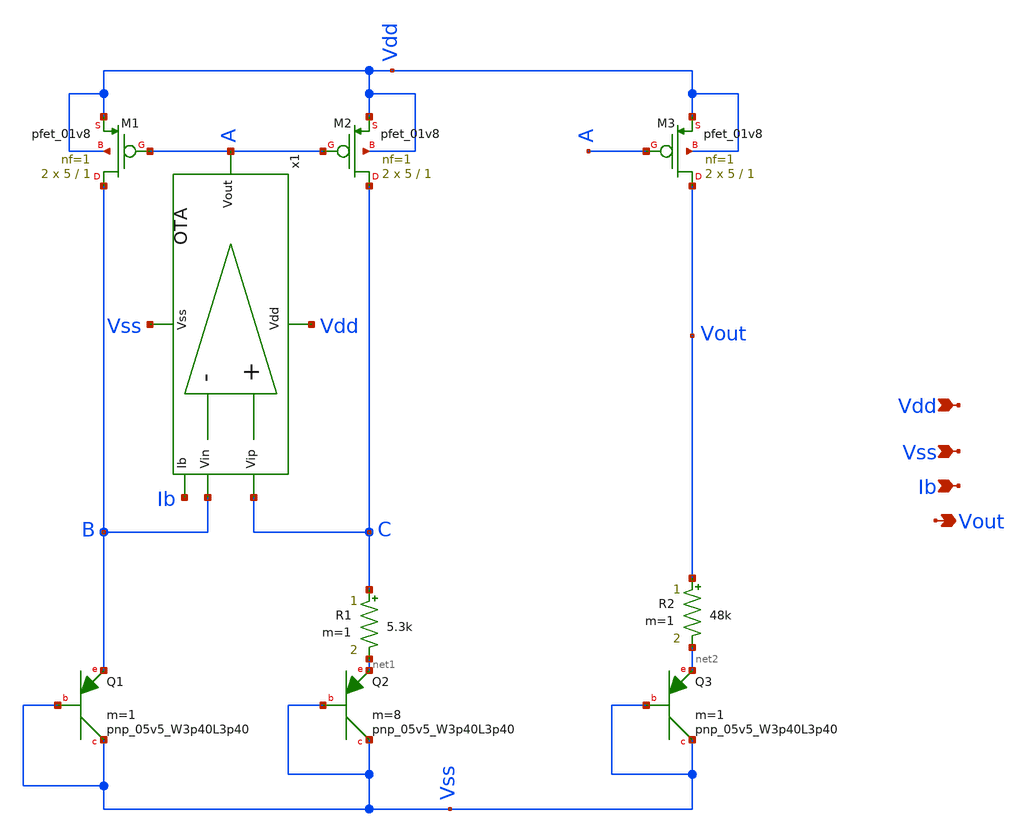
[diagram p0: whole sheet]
** sch_path: temp_sensor_sky130nm/design/TEMP_SENSOR_SKY130NM/BGR.sch
**.subckt BGR Vdd Vss Ib Vout
*.ipin Vdd
*.ipin Vss
*.ipin Ib
*.opin Vout
XM1 B A Vdd Vdd sky130_fd_pr__pfet_01v8 L=1 W=5 nf=1 ad='int((nf+1)/2) * W/nf * 0.29' as='int((nf+2)/2) * W/nf * 0.29'
+ pd='2*int((nf+1)/2) * (W/nf + 0.29)' ps='2*int((nf+2)/2) * (W/nf + 0.29)' nrd='0.29 / W' nrs='0.29 / W'
+ sa=0 sb=0 sd=0 mult=2 m=2
XM2 C A Vdd Vdd sky130_fd_pr__pfet_01v8 L=1 W=5 nf=1 ad='int((nf+1)/2) * W/nf * 0.29' as='int((nf+2)/2) * W/nf * 0.29'
+ pd='2*int((nf+1)/2) * (W/nf + 0.29)' ps='2*int((nf+2)/2) * (W/nf + 0.29)' nrd='0.29 / W' nrs='0.29 / W'
+ sa=0 sb=0 sd=0 mult=2 m=2
XQ1 Vss Vss B sky130_fd_pr__pnp_05v5_W3p40L3p40 m=1
XQ2 Vss Vss net1 sky130_fd_pr__pnp_05v5_W3p40L3p40 m=8
XQ3 Vss Vss net2 sky130_fd_pr__pnp_05v5_W3p40L3p40 m=1
XM3 Vout A Vdd Vdd sky130_fd_pr__pfet_01v8 L=1 W=5 nf=1 ad='int((nf+1)/2) * W/nf * 0.29' as='int((nf+2)/2) * W/nf * 0.29'
+ pd='2*int((nf+1)/2) * (W/nf + 0.29)' ps='2*int((nf+2)/2) * (W/nf + 0.29)' nrd='0.29 / W' nrs='0.29 / W'
+ sa=0 sb=0 sd=0 mult=2 m=2
R1 C net1 5.3k m=1
R2 Vout net2 48k m=1
x1 Vdd Vss C B Ib A OTA
**.ends

* expanding   symbol:  TEMP_SENSOR_SKY130NM/OTA.sym # of pins=6
** sym_path: temp_sensor_sky130nm/design/TEMP_SENSOR_SKY130NM/OTA.sym
** sch_path: temp_sensor_sky130nm/design/TEMP_SENSOR_SKY130NM/OTA.sch
.subckt OTA Vdd Vss Vip Vin Ib Vout
*.ipin Vdd
*.ipin Vss
*.ipin Vip
*.ipin Vin
*.ipin Ib
*.opin Vout
Cc Vout net3 800f m=1
XM1 net2 Vin net1 net1 sky130_fd_pr__pfet_01v8 L=1 W=3 nf=1 ad='int((nf+1)/2) * W/nf * 0.29' as='int((nf+2)/2) * W/nf * 0.29'
+ pd='2*int((nf+1)/2) * (W/nf + 0.29)' ps='2*int((nf+2)/2) * (W/nf + 0.29)' nrd='0.29 / W' nrs='0.29 / W'
+ sa=0 sb=0 sd=0 mult=1 m=1
XM2 net3 Vip net1 net1 sky130_fd_pr__pfet_01v8 L=1 W=3 nf=1 ad='int((nf+1)/2) * W/nf * 0.29' as='int((nf+2)/2) * W/nf * 0.29'
+ pd='2*int((nf+1)/2) * (W/nf + 0.29)' ps='2*int((nf+2)/2) * (W/nf + 0.29)' nrd='0.29 / W' nrs='0.29 / W'
+ sa=0 sb=0 sd=0 mult=1 m=1
XM3 net2 net2 Vss Vss sky130_fd_pr__nfet_01v8 L=1 W=1 nf=1 ad='int((nf+1)/2) * W/nf * 0.29' as='int((nf+2)/2) * W/nf * 0.29'
+ pd='2*int((nf+1)/2) * (W/nf + 0.29)' ps='2*int((nf+2)/2) * (W/nf + 0.29)' nrd='0.29 / W' nrs='0.29 / W'
+ sa=0 sb=0 sd=0 mult=1 m=1
XM4 net3 net2 Vss Vss sky130_fd_pr__nfet_01v8 L=1 W=1 nf=1 ad='int((nf+1)/2) * W/nf * 0.29' as='int((nf+2)/2) * W/nf * 0.29'
+ pd='2*int((nf+1)/2) * (W/nf + 0.29)' ps='2*int((nf+2)/2) * (W/nf + 0.29)' nrd='0.29 / W' nrs='0.29 / W'
+ sa=0 sb=0 sd=0 mult=1 m=1
XM5 net1 Ib Vdd Vdd sky130_fd_pr__pfet_01v8 L=1 W=6 nf=1 ad='int((nf+1)/2) * W/nf * 0.29' as='int((nf+2)/2) * W/nf * 0.29'
+ pd='2*int((nf+1)/2) * (W/nf + 0.29)' ps='2*int((nf+2)/2) * (W/nf + 0.29)' nrd='0.29 / W' nrs='0.29 / W'
+ sa=0 sb=0 sd=0 mult=1 m=1
XM6 Vout Ib Vdd Vdd sky130_fd_pr__pfet_01v8 L=1 W=6 nf=1 ad='int((nf+1)/2) * W/nf * 0.29' as='int((nf+2)/2) * W/nf * 0.29'
+ pd='2*int((nf+1)/2) * (W/nf + 0.29)' ps='2*int((nf+2)/2) * (W/nf + 0.29)' nrd='0.29 / W' nrs='0.29 / W'
+ sa=0 sb=0 sd=0 mult=1 m=1
XM7 Vout net3 Vss Vss sky130_fd_pr__nfet_01v8 L=1 W=2 nf=1 ad='int((nf+1)/2) * W/nf * 0.29' as='int((nf+2)/2) * W/nf * 0.29'
+ pd='2*int((nf+1)/2) * (W/nf + 0.29)' ps='2*int((nf+2)/2) * (W/nf + 0.29)' nrd='0.29 / W' nrs='0.29 / W'
+ sa=0 sb=0 sd=0 mult=1 m=1
XM8 Ib Ib Vdd Vdd sky130_fd_pr__pfet_01v8 L=1 W=6 nf=1 ad='int((nf+1)/2) * W/nf * 0.29' as='int((nf+2)/2) * W/nf * 0.29'
+ pd='2*int((nf+1)/2) * (W/nf + 0.29)' ps='2*int((nf+2)/2) * (W/nf + 0.29)' nrd='0.29 / W' nrs='0.29 / W'
+ sa=0 sb=0 sd=0 mult=1 m=1
.ends

.end
